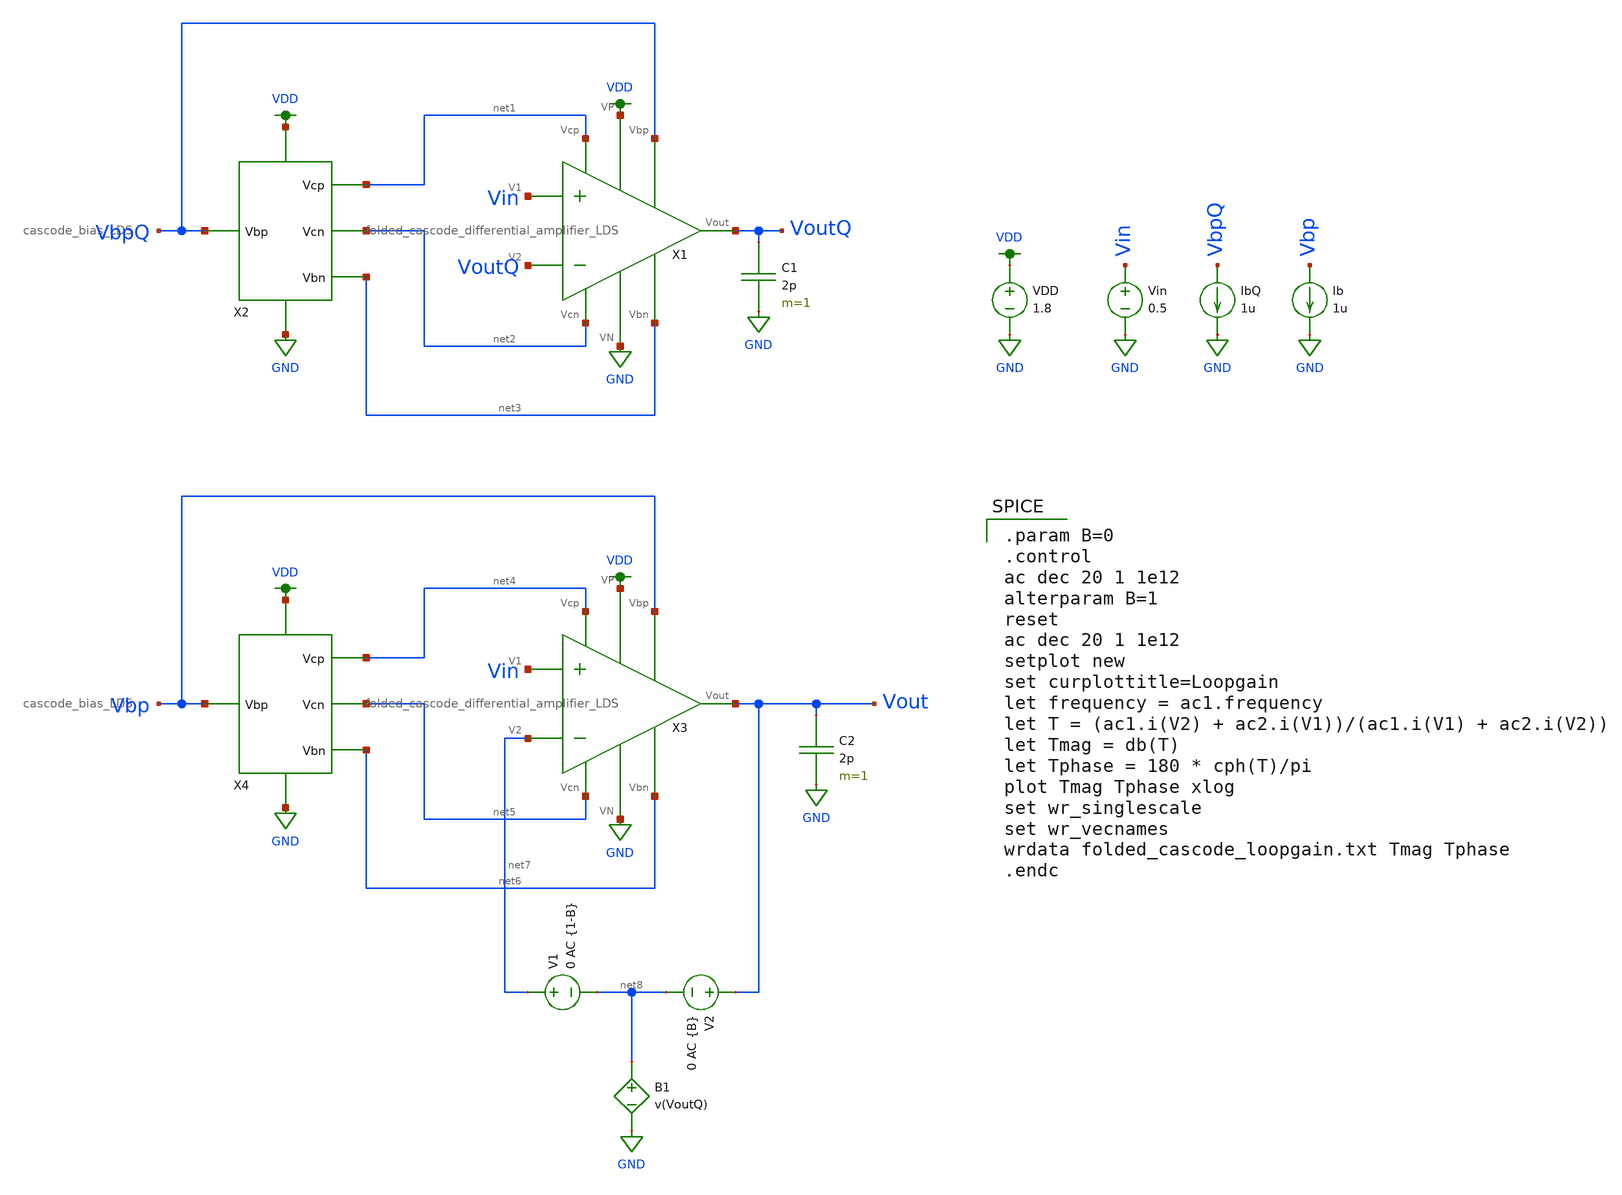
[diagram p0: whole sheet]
** sch_path: schematic/folded_cascode_loopgain_simulation.sch
**.subckt folded_cascode_loopgain_simulation
X1 VDD VbpQ net1 VoutQ net3 net2 Vin VoutQ GND folded_cascode_differential_amplifier_LDS
X2 VDD net1 VbpQ net2 net3 GND cascode_bias_LDS
VDD VDD GND 1.8
Vin Vin GND 0.5
IbQ VbpQ GND 1u
C1 VoutQ GND 2p m=1
Ib Vbp GND 1u
X3 VDD Vbp net4 Vout net6 net5 Vin net7 GND folded_cascode_differential_amplifier_LDS
X4 VDD net4 Vbp net5 net6 GND cascode_bias_LDS
C2 Vout GND 2p m=1
V1 net7 net8 0 AC {1-B}
V2 Vout net8 0 AC {B}
B1 net8 GND V=v(VoutQ)
**** begin user architecture code

.option wnflag=1
.lib ~/skywater/skywater-pdk/libraries/sky130_fd_pr_ngspice/latest/models/sky130.lib.spice tt


.param B=0
.control
ac dec 20 1 1e12
alterparam B=1
reset
ac dec 20 1 1e12
setplot new
set curplottitle=Loopgain
let frequency = ac1.frequency
let T = (ac1.i(V2) + ac2.i(V1))/(ac1.i(V1) + ac2.i(V2))
let Tmag = db(T)
let Tphase = 180 * cph(T)/pi
plot Tmag Tphase xlog
set wr_singlescale
set wr_vecnames
wrdata folded_cascode_loopgain.txt Tmag Tphase
.endc

**** end user architecture code
**.ends

* expanding   symbol:
*+  /home/madvlsi/Documents/MADVLSI-MP3/schematic/folded_cascode_differential_amplifier_LDS.sym # of pins=9
** sym_path: schematic/folded_cascode_differential_amplifier_LDS.sym
** sch_path: schematic/folded_cascode_differential_amplifier_LDS.sch
.subckt folded_cascode_differential_amplifier_LDS VP Vbp Vcp Vout Vbn Vcn V1 V2 VN
*.ipin Vbn
*.ipin Vcn
*.ipin Vcp
*.ipin V2
*.ipin V1
*.ipin Vbp
*.iopin Vp
*.iopin Vn
*.opin Vout
XM11 net3 Vcn net6 GND sky130_fd_pr__nfet_01v8 L=0.5 W=12 nf=1 ad='int((nf+1)/2) * W/nf * 0.29' as='int((nf+2)/2) * W/nf * 0.29'
+ pd='2*int((nf+1)/2) * (W/nf + 0.29)' ps='2*int((nf+2)/2) * (W/nf + 0.29)' nrd='0.29 / W' nrs='0.29 / W'
+ sa=0 sb=0 sd=0 mult=1 m=1
XM12 net3 V1 net1 VDD sky130_fd_pr__pfet_01v8 L=0.5 W=12 nf=1 ad='int((nf+1)/2) * W/nf * 0.29' as='int((nf+2)/2) * W/nf * 0.29'
+ pd='2*int((nf+1)/2) * (W/nf + 0.29)' ps='2*int((nf+2)/2) * (W/nf + 0.29)' nrd='0.29 / W' nrs='0.29 / W'
+ sa=0 sb=0 sd=0 mult=1 m=1
XM13 net2 V2 net1 VDD sky130_fd_pr__pfet_01v8 L=0.5 W=12 nf=1 ad='int((nf+1)/2) * W/nf * 0.29' as='int((nf+2)/2) * W/nf * 0.29'
+ pd='2*int((nf+1)/2) * (W/nf + 0.29)' ps='2*int((nf+2)/2) * (W/nf + 0.29)' nrd='0.29 / W' nrs='0.29 / W'
+ sa=0 sb=0 sd=0 mult=1 m=1
XM14 net1 V2 net2 VDD sky130_fd_pr__pfet_01v8 L=0.5 W=12 nf=1 ad='int((nf+1)/2) * W/nf * 0.29' as='int((nf+2)/2) * W/nf * 0.29'
+ pd='2*int((nf+1)/2) * (W/nf + 0.29)' ps='2*int((nf+2)/2) * (W/nf + 0.29)' nrd='0.29 / W' nrs='0.29 / W'
+ sa=0 sb=0 sd=0 mult=1 m=1
XM15 net1 V1 net3 VDD sky130_fd_pr__pfet_01v8 L=0.5 W=12 nf=1 ad='int((nf+1)/2) * W/nf * 0.29' as='int((nf+2)/2) * W/nf * 0.29'
+ pd='2*int((nf+1)/2) * (W/nf + 0.29)' ps='2*int((nf+2)/2) * (W/nf + 0.29)' nrd='0.29 / W' nrs='0.29 / W'
+ sa=0 sb=0 sd=0 mult=1 m=1
XM16 net3 V1 net1 VDD sky130_fd_pr__pfet_01v8 L=0.5 W=12 nf=1 ad='int((nf+1)/2) * W/nf * 0.29' as='int((nf+2)/2) * W/nf * 0.29'
+ pd='2*int((nf+1)/2) * (W/nf + 0.29)' ps='2*int((nf+2)/2) * (W/nf + 0.29)' nrd='0.29 / W' nrs='0.29 / W'
+ sa=0 sb=0 sd=0 mult=1 m=1
XM17 net2 V2 net1 VDD sky130_fd_pr__pfet_01v8 L=0.5 W=12 nf=1 ad='int((nf+1)/2) * W/nf * 0.29' as='int((nf+2)/2) * W/nf * 0.29'
+ pd='2*int((nf+1)/2) * (W/nf + 0.29)' ps='2*int((nf+2)/2) * (W/nf + 0.29)' nrd='0.29 / W' nrs='0.29 / W'
+ sa=0 sb=0 sd=0 mult=1 m=1
XM18 net1 V2 net2 VDD sky130_fd_pr__pfet_01v8 L=0.5 W=12 nf=1 ad='int((nf+1)/2) * W/nf * 0.29' as='int((nf+2)/2) * W/nf * 0.29'
+ pd='2*int((nf+1)/2) * (W/nf + 0.29)' ps='2*int((nf+2)/2) * (W/nf + 0.29)' nrd='0.29 / W' nrs='0.29 / W'
+ sa=0 sb=0 sd=0 mult=1 m=1
XM19 net1 V1 net3 VDD sky130_fd_pr__pfet_01v8 L=0.5 W=12 nf=1 ad='int((nf+1)/2) * W/nf * 0.29' as='int((nf+2)/2) * W/nf * 0.29'
+ pd='2*int((nf+1)/2) * (W/nf + 0.29)' ps='2*int((nf+2)/2) * (W/nf + 0.29)' nrd='0.29 / W' nrs='0.29 / W'
+ sa=0 sb=0 sd=0 mult=1 m=1
XM20 Vp Vbp net1 VDD sky130_fd_pr__pfet_01v8 L=0.5 W=12 nf=1 ad='int((nf+1)/2) * W/nf * 0.29' as='int((nf+2)/2) * W/nf * 0.29'
+ pd='2*int((nf+1)/2) * (W/nf + 0.29)' ps='2*int((nf+2)/2) * (W/nf + 0.29)' nrd='0.29 / W' nrs='0.29 / W'
+ sa=0 sb=0 sd=0 mult=1 m=1
XM21 net1 Vbp Vp VDD sky130_fd_pr__pfet_01v8 L=0.5 W=12 nf=1 ad='int((nf+1)/2) * W/nf * 0.29' as='int((nf+2)/2) * W/nf * 0.29'
+ pd='2*int((nf+1)/2) * (W/nf + 0.29)' ps='2*int((nf+2)/2) * (W/nf + 0.29)' nrd='0.29 / W' nrs='0.29 / W'
+ sa=0 sb=0 sd=0 mult=1 m=1
XM22 Vp Vbp net1 VDD sky130_fd_pr__pfet_01v8 L=0.5 W=12 nf=1 ad='int((nf+1)/2) * W/nf * 0.29' as='int((nf+2)/2) * W/nf * 0.29'
+ pd='2*int((nf+1)/2) * (W/nf + 0.29)' ps='2*int((nf+2)/2) * (W/nf + 0.29)' nrd='0.29 / W' nrs='0.29 / W'
+ sa=0 sb=0 sd=0 mult=1 m=1
XM23 net1 Vbp Vp VDD sky130_fd_pr__pfet_01v8 L=0.5 W=12 nf=1 ad='int((nf+1)/2) * W/nf * 0.29' as='int((nf+2)/2) * W/nf * 0.29'
+ pd='2*int((nf+1)/2) * (W/nf + 0.29)' ps='2*int((nf+2)/2) * (W/nf + 0.29)' nrd='0.29 / W' nrs='0.29 / W'
+ sa=0 sb=0 sd=0 mult=1 m=1
XM24 Vp Vbp net1 VDD sky130_fd_pr__pfet_01v8 L=0.5 W=12 nf=1 ad='int((nf+1)/2) * W/nf * 0.29' as='int((nf+2)/2) * W/nf * 0.29'
+ pd='2*int((nf+1)/2) * (W/nf + 0.29)' ps='2*int((nf+2)/2) * (W/nf + 0.29)' nrd='0.29 / W' nrs='0.29 / W'
+ sa=0 sb=0 sd=0 mult=1 m=1
XM25 net1 Vbp Vp VDD sky130_fd_pr__pfet_01v8 L=0.5 W=12 nf=1 ad='int((nf+1)/2) * W/nf * 0.29' as='int((nf+2)/2) * W/nf * 0.29'
+ pd='2*int((nf+1)/2) * (W/nf + 0.29)' ps='2*int((nf+2)/2) * (W/nf + 0.29)' nrd='0.29 / W' nrs='0.29 / W'
+ sa=0 sb=0 sd=0 mult=1 m=1
XM26 Vp Vbp net1 VDD sky130_fd_pr__pfet_01v8 L=0.5 W=12 nf=1 ad='int((nf+1)/2) * W/nf * 0.29' as='int((nf+2)/2) * W/nf * 0.29'
+ pd='2*int((nf+1)/2) * (W/nf + 0.29)' ps='2*int((nf+2)/2) * (W/nf + 0.29)' nrd='0.29 / W' nrs='0.29 / W'
+ sa=0 sb=0 sd=0 mult=1 m=1
XM27 net1 Vbp Vp VDD sky130_fd_pr__pfet_01v8 L=0.5 W=12 nf=1 ad='int((nf+1)/2) * W/nf * 0.29' as='int((nf+2)/2) * W/nf * 0.29'
+ pd='2*int((nf+1)/2) * (W/nf + 0.29)' ps='2*int((nf+2)/2) * (W/nf + 0.29)' nrd='0.29 / W' nrs='0.29 / W'
+ sa=0 sb=0 sd=0 mult=1 m=1
XM36 Vn Vbn net3 GND sky130_fd_pr__nfet_01v8 L=0.5 W=12 nf=1 ad='int((nf+1)/2) * W/nf * 0.29' as='int((nf+2)/2) * W/nf * 0.29'
+ pd='2*int((nf+1)/2) * (W/nf + 0.29)' ps='2*int((nf+2)/2) * (W/nf + 0.29)' nrd='0.29 / W' nrs='0.29 / W'
+ sa=0 sb=0 sd=0 mult=1 m=1
XM37 net2 Vbn Vn GND sky130_fd_pr__nfet_01v8 L=0.5 W=12 nf=1 ad='int((nf+1)/2) * W/nf * 0.29' as='int((nf+2)/2) * W/nf * 0.29'
+ pd='2*int((nf+1)/2) * (W/nf + 0.29)' ps='2*int((nf+2)/2) * (W/nf + 0.29)' nrd='0.29 / W' nrs='0.29 / W'
+ sa=0 sb=0 sd=0 mult=1 m=1
XM38 Vout Vcn net2 GND sky130_fd_pr__nfet_01v8 L=0.5 W=12 nf=1 ad='int((nf+1)/2) * W/nf * 0.29' as='int((nf+2)/2) * W/nf * 0.29'
+ pd='2*int((nf+1)/2) * (W/nf + 0.29)' ps='2*int((nf+2)/2) * (W/nf + 0.29)' nrd='0.29 / W' nrs='0.29 / W'
+ sa=0 sb=0 sd=0 mult=1 m=1
XM39 net2 Vcn Vout GND sky130_fd_pr__nfet_01v8 L=0.5 W=12 nf=1 ad='int((nf+1)/2) * W/nf * 0.29' as='int((nf+2)/2) * W/nf * 0.29'
+ pd='2*int((nf+1)/2) * (W/nf + 0.29)' ps='2*int((nf+2)/2) * (W/nf + 0.29)' nrd='0.29 / W' nrs='0.29 / W'
+ sa=0 sb=0 sd=0 mult=1 m=1
XM40 Vn Vbn net2 GND sky130_fd_pr__nfet_01v8 L=0.5 W=12 nf=1 ad='int((nf+1)/2) * W/nf * 0.29' as='int((nf+2)/2) * W/nf * 0.29'
+ pd='2*int((nf+1)/2) * (W/nf + 0.29)' ps='2*int((nf+2)/2) * (W/nf + 0.29)' nrd='0.29 / W' nrs='0.29 / W'
+ sa=0 sb=0 sd=0 mult=1 m=1
XM41 net3 Vbn Vn GND sky130_fd_pr__nfet_01v8 L=0.5 W=12 nf=1 ad='int((nf+1)/2) * W/nf * 0.29' as='int((nf+2)/2) * W/nf * 0.29'
+ pd='2*int((nf+1)/2) * (W/nf + 0.29)' ps='2*int((nf+2)/2) * (W/nf + 0.29)' nrd='0.29 / W' nrs='0.29 / W'
+ sa=0 sb=0 sd=0 mult=1 m=1
XM42 net6 Vcn net3 GND sky130_fd_pr__nfet_01v8 L=0.5 W=12 nf=1 ad='int((nf+1)/2) * W/nf * 0.29' as='int((nf+2)/2) * W/nf * 0.29'
+ pd='2*int((nf+1)/2) * (W/nf + 0.29)' ps='2*int((nf+2)/2) * (W/nf + 0.29)' nrd='0.29 / W' nrs='0.29 / W'
+ sa=0 sb=0 sd=0 mult=1 m=1
XM44 Vout Vcp net4 VDD sky130_fd_pr__pfet_01v8 L=0.5 W=12 nf=1 ad='int((nf+1)/2) * W/nf * 0.29' as='int((nf+2)/2) * W/nf * 0.29'
+ pd='2*int((nf+1)/2) * (W/nf + 0.29)' ps='2*int((nf+2)/2) * (W/nf + 0.29)' nrd='0.29 / W' nrs='0.29 / W'
+ sa=0 sb=0 sd=0 mult=1 m=1
XM45 net4 net6 Vp VDD sky130_fd_pr__pfet_01v8 L=0.5 W=12 nf=1 ad='int((nf+1)/2) * W/nf * 0.29' as='int((nf+2)/2) * W/nf * 0.29'
+ pd='2*int((nf+1)/2) * (W/nf + 0.29)' ps='2*int((nf+2)/2) * (W/nf + 0.29)' nrd='0.29 / W' nrs='0.29 / W'
+ sa=0 sb=0 sd=0 mult=1 m=1
XM46 Vp net6 net5 VDD sky130_fd_pr__pfet_01v8 L=0.5 W=12 nf=1 ad='int((nf+1)/2) * W/nf * 0.29' as='int((nf+2)/2) * W/nf * 0.29'
+ pd='2*int((nf+1)/2) * (W/nf + 0.29)' ps='2*int((nf+2)/2) * (W/nf + 0.29)' nrd='0.29 / W' nrs='0.29 / W'
+ sa=0 sb=0 sd=0 mult=1 m=1
XM47 net5 Vcp net6 VDD sky130_fd_pr__pfet_01v8 L=0.5 W=12 nf=1 ad='int((nf+1)/2) * W/nf * 0.29' as='int((nf+2)/2) * W/nf * 0.29'
+ pd='2*int((nf+1)/2) * (W/nf + 0.29)' ps='2*int((nf+2)/2) * (W/nf + 0.29)' nrd='0.29 / W' nrs='0.29 / W'
+ sa=0 sb=0 sd=0 mult=1 m=1
XM48 net6 Vcp net5 VDD sky130_fd_pr__pfet_01v8 L=0.5 W=12 nf=1 ad='int((nf+1)/2) * W/nf * 0.29' as='int((nf+2)/2) * W/nf * 0.29'
+ pd='2*int((nf+1)/2) * (W/nf + 0.29)' ps='2*int((nf+2)/2) * (W/nf + 0.29)' nrd='0.29 / W' nrs='0.29 / W'
+ sa=0 sb=0 sd=0 mult=1 m=1
XM49 net5 net6 Vp VDD sky130_fd_pr__pfet_01v8 L=0.5 W=12 nf=1 ad='int((nf+1)/2) * W/nf * 0.29' as='int((nf+2)/2) * W/nf * 0.29'
+ pd='2*int((nf+1)/2) * (W/nf + 0.29)' ps='2*int((nf+2)/2) * (W/nf + 0.29)' nrd='0.29 / W' nrs='0.29 / W'
+ sa=0 sb=0 sd=0 mult=1 m=1
XM50 Vp net6 net4 VDD sky130_fd_pr__pfet_01v8 L=0.5 W=12 nf=1 ad='int((nf+1)/2) * W/nf * 0.29' as='int((nf+2)/2) * W/nf * 0.29'
+ pd='2*int((nf+1)/2) * (W/nf + 0.29)' ps='2*int((nf+2)/2) * (W/nf + 0.29)' nrd='0.29 / W' nrs='0.29 / W'
+ sa=0 sb=0 sd=0 mult=1 m=1
XM51 net4 Vcp Vout VDD sky130_fd_pr__pfet_01v8 L=0.5 W=12 nf=1 ad='int((nf+1)/2) * W/nf * 0.29' as='int((nf+2)/2) * W/nf * 0.29'
+ pd='2*int((nf+1)/2) * (W/nf + 0.29)' ps='2*int((nf+2)/2) * (W/nf + 0.29)' nrd='0.29 / W' nrs='0.29 / W'
+ sa=0 sb=0 sd=0 mult=1 m=1
.ends


* expanding   symbol:  /home/madvlsi/Documents/MADVLSI-MP3/schematic/cascode_bias_LDS.sym # of
*+ pins=6
** sym_path: schematic/cascode_bias_LDS.sym
** sch_path: schematic/cascode_bias_LDS.sch
.subckt cascode_bias_LDS VP Vcp Vbp Vcn Vbn VN
*.iopin VP
*.iopin VN
*.opin Vcp
*.opin Vbn
*.opin Vcn
*.iopin Vbp
XM1a VP Vbp Vbp VDD sky130_fd_pr__pfet_01v8 L=0.5 W=6 nf=1 ad='int((nf+1)/2) * W/nf * 0.29' as='int((nf+2)/2) * W/nf * 0.29'
+ pd='2*int((nf+1)/2) * (W/nf + 0.29)' ps='2*int((nf+2)/2) * (W/nf + 0.29)' nrd='0.29 / W' nrs='0.29 / W'
+ sa=0 sb=0 sd=0 mult=1 m=1
XM2a Vbn Vbp VP VDD sky130_fd_pr__pfet_01v8 L=0.5 W=6 nf=1 ad='int((nf+1)/2) * W/nf * 0.29' as='int((nf+2)/2) * W/nf * 0.29'
+ pd='2*int((nf+1)/2) * (W/nf + 0.29)' ps='2*int((nf+2)/2) * (W/nf + 0.29)' nrd='0.29 / W' nrs='0.29 / W'
+ sa=0 sb=0 sd=0 mult=1 m=1
XM3a VP Vbp Vcn VDD sky130_fd_pr__pfet_01v8 L=0.5 W=6 nf=1 ad='int((nf+1)/2) * W/nf * 0.29' as='int((nf+2)/2) * W/nf * 0.29'
+ pd='2*int((nf+1)/2) * (W/nf + 0.29)' ps='2*int((nf+2)/2) * (W/nf + 0.29)' nrd='0.29 / W' nrs='0.29 / W'
+ sa=0 sb=0 sd=0 mult=1 m=1
XM4a net1 Vbp VP VDD sky130_fd_pr__pfet_01v8 L=0.5 W=6 nf=1 ad='int((nf+1)/2) * W/nf * 0.29' as='int((nf+2)/2) * W/nf * 0.29'
+ pd='2*int((nf+1)/2) * (W/nf + 0.29)' ps='2*int((nf+2)/2) * (W/nf + 0.29)' nrd='0.29 / W' nrs='0.29 / W'
+ sa=0 sb=0 sd=0 mult=1 m=1
XM4c net2 Vbp net3 VDD sky130_fd_pr__pfet_01v8 L=0.5 W=6 nf=1 ad='int((nf+1)/2) * W/nf * 0.29' as='int((nf+2)/2) * W/nf * 0.29'
+ pd='2*int((nf+1)/2) * (W/nf + 0.29)' ps='2*int((nf+2)/2) * (W/nf + 0.29)' nrd='0.29 / W' nrs='0.29 / W'
+ sa=0 sb=0 sd=0 mult=1 m=1
XM3b Vcn Vbp VP VDD sky130_fd_pr__pfet_01v8 L=0.5 W=6 nf=1 ad='int((nf+1)/2) * W/nf * 0.29' as='int((nf+2)/2) * W/nf * 0.29'
+ pd='2*int((nf+1)/2) * (W/nf + 0.29)' ps='2*int((nf+2)/2) * (W/nf + 0.29)' nrd='0.29 / W' nrs='0.29 / W'
+ sa=0 sb=0 sd=0 mult=1 m=1
XM2b VP Vbp Vbn VDD sky130_fd_pr__pfet_01v8 L=0.5 W=6 nf=1 ad='int((nf+1)/2) * W/nf * 0.29' as='int((nf+2)/2) * W/nf * 0.29'
+ pd='2*int((nf+1)/2) * (W/nf + 0.29)' ps='2*int((nf+2)/2) * (W/nf + 0.29)' nrd='0.29 / W' nrs='0.29 / W'
+ sa=0 sb=0 sd=0 mult=1 m=1
XM1b Vbp Vbp VP VDD sky130_fd_pr__pfet_01v8 L=0.5 W=6 nf=1 ad='int((nf+1)/2) * W/nf * 0.29' as='int((nf+2)/2) * W/nf * 0.29'
+ pd='2*int((nf+1)/2) * (W/nf + 0.29)' ps='2*int((nf+2)/2) * (W/nf + 0.29)' nrd='0.29 / W' nrs='0.29 / W'
+ sa=0 sb=0 sd=0 mult=1 m=1
XM6a net5 net5 net4 VDD sky130_fd_pr__pfet_01v8 L=0.5 W=6 nf=1 ad='int((nf+1)/2) * W/nf * 0.29' as='int((nf+2)/2) * W/nf * 0.29'
+ pd='2*int((nf+1)/2) * (W/nf + 0.29)' ps='2*int((nf+2)/2) * (W/nf + 0.29)' nrd='0.29 / W' nrs='0.29 / W'
+ sa=0 sb=0 sd=0 mult=1 m=1
XM6b net5 net5 net5 VDD sky130_fd_pr__pfet_01v8 L=0.5 W=6 nf=1 ad='int((nf+1)/2) * W/nf * 0.29' as='int((nf+2)/2) * W/nf * 0.29'
+ pd='2*int((nf+1)/2) * (W/nf + 0.29)' ps='2*int((nf+2)/2) * (W/nf + 0.29)' nrd='0.29 / W' nrs='0.29 / W'
+ sa=0 sb=0 sd=0 mult=1 m=1
XM5a Vcp Vcp net4 VDD sky130_fd_pr__pfet_01v8 L=0.5 W=6 nf=1 ad='int((nf+1)/2) * W/nf * 0.29' as='int((nf+2)/2) * W/nf * 0.29'
+ pd='2*int((nf+1)/2) * (W/nf + 0.29)' ps='2*int((nf+2)/2) * (W/nf + 0.29)' nrd='0.29 / W' nrs='0.29 / W'
+ sa=0 sb=0 sd=0 mult=1 m=1
XM5b net4 Vcp Vcp VDD sky130_fd_pr__pfet_01v8 L=0.5 W=6 nf=1 ad='int((nf+1)/2) * W/nf * 0.29' as='int((nf+2)/2) * W/nf * 0.29'
+ pd='2*int((nf+1)/2) * (W/nf + 0.29)' ps='2*int((nf+2)/2) * (W/nf + 0.29)' nrd='0.29 / W' nrs='0.29 / W'
+ sa=0 sb=0 sd=0 mult=1 m=1
XM6c net5 net5 net5 VDD sky130_fd_pr__pfet_01v8 L=0.5 W=6 nf=1 ad='int((nf+1)/2) * W/nf * 0.29' as='int((nf+2)/2) * W/nf * 0.29'
+ pd='2*int((nf+1)/2) * (W/nf + 0.29)' ps='2*int((nf+2)/2) * (W/nf + 0.29)' nrd='0.29 / W' nrs='0.29 / W'
+ sa=0 sb=0 sd=0 mult=1 m=1
XM6d net4 net5 net5 VDD sky130_fd_pr__pfet_01v8 L=0.5 W=6 nf=1 ad='int((nf+1)/2) * W/nf * 0.29' as='int((nf+2)/2) * W/nf * 0.29'
+ pd='2*int((nf+1)/2) * (W/nf + 0.29)' ps='2*int((nf+2)/2) * (W/nf + 0.29)' nrd='0.29 / W' nrs='0.29 / W'
+ sa=0 sb=0 sd=0 mult=1 m=1
XM8a Vcp Vbn VN GND sky130_fd_pr__nfet_01v8 L=0.5 W=6 nf=1 ad='int((nf+1)/2) * W/nf * 0.29' as='int((nf+2)/2) * W/nf * 0.29'
+ pd='2*int((nf+1)/2) * (W/nf + 0.29)' ps='2*int((nf+2)/2) * (W/nf + 0.29)' nrd='0.29 / W' nrs='0.29 / W'
+ sa=0 sb=0 sd=0 mult=1 m=1
XM8b VN Vbn Vcp GND sky130_fd_pr__nfet_01v8 L=0.5 W=6 nf=1 ad='int((nf+1)/2) * W/nf * 0.29' as='int((nf+2)/2) * W/nf * 0.29'
+ pd='2*int((nf+1)/2) * (W/nf + 0.29)' ps='2*int((nf+2)/2) * (W/nf + 0.29)' nrd='0.29 / W' nrs='0.29 / W'
+ sa=0 sb=0 sd=0 mult=1 m=1
XM10b VN Vbn net6 GND sky130_fd_pr__nfet_01v8 L=0.5 W=6 nf=1 ad='int((nf+1)/2) * W/nf * 0.29' as='int((nf+2)/2) * W/nf * 0.29'
+ pd='2*int((nf+1)/2) * (W/nf + 0.29)' ps='2*int((nf+2)/2) * (W/nf + 0.29)' nrd='0.29 / W' nrs='0.29 / W'
+ sa=0 sb=0 sd=0 mult=1 m=1
XM9a Vbn Vbn VN GND sky130_fd_pr__nfet_01v8 L=0.5 W=6 nf=1 ad='int((nf+1)/2) * W/nf * 0.29' as='int((nf+2)/2) * W/nf * 0.29'
+ pd='2*int((nf+1)/2) * (W/nf + 0.29)' ps='2*int((nf+2)/2) * (W/nf + 0.29)' nrd='0.29 / W' nrs='0.29 / W'
+ sa=0 sb=0 sd=0 mult=1 m=1
XM9b VN Vbn Vbn GND sky130_fd_pr__nfet_01v8 L=0.5 W=6 nf=1 ad='int((nf+1)/2) * W/nf * 0.29' as='int((nf+2)/2) * W/nf * 0.29'
+ pd='2*int((nf+1)/2) * (W/nf + 0.29)' ps='2*int((nf+2)/2) * (W/nf + 0.29)' nrd='0.29 / W' nrs='0.29 / W'
+ sa=0 sb=0 sd=0 mult=1 m=1
XM10c net6 Vbn VN GND sky130_fd_pr__nfet_01v8 L=0.5 W=6 nf=1 ad='int((nf+1)/2) * W/nf * 0.29' as='int((nf+2)/2) * W/nf * 0.29'
+ pd='2*int((nf+1)/2) * (W/nf + 0.29)' ps='2*int((nf+2)/2) * (W/nf + 0.29)' nrd='0.29 / W' nrs='0.29 / W'
+ sa=0 sb=0 sd=0 mult=1 m=1
XM11a Vcn Vcn net7 GND sky130_fd_pr__nfet_01v8 L=0.5 W=6 nf=1 ad='int((nf+1)/2) * W/nf * 0.29' as='int((nf+2)/2) * W/nf * 0.29'
+ pd='2*int((nf+1)/2) * (W/nf + 0.29)' ps='2*int((nf+2)/2) * (W/nf + 0.29)' nrd='0.29 / W' nrs='0.29 / W'
+ sa=0 sb=0 sd=0 mult=1 m=1
XM11b net7 Vcn Vcn GND sky130_fd_pr__nfet_01v8 L=0.5 W=6 nf=1 ad='int((nf+1)/2) * W/nf * 0.29' as='int((nf+2)/2) * W/nf * 0.29'
+ pd='2*int((nf+1)/2) * (W/nf + 0.29)' ps='2*int((nf+2)/2) * (W/nf + 0.29)' nrd='0.29 / W' nrs='0.29 / W'
+ sa=0 sb=0 sd=0 mult=1 m=1
XM13a net7 net3 VN GND sky130_fd_pr__nfet_01v8 L=0.5 W=6 nf=1 ad='int((nf+1)/2) * W/nf * 0.29' as='int((nf+2)/2) * W/nf * 0.29'
+ pd='2*int((nf+1)/2) * (W/nf + 0.29)' ps='2*int((nf+2)/2) * (W/nf + 0.29)' nrd='0.29 / W' nrs='0.29 / W'
+ sa=0 sb=0 sd=0 mult=1 m=1
XM12a net3 net3 net7 GND sky130_fd_pr__nfet_01v8 L=0.5 W=6 nf=1 ad='int((nf+1)/2) * W/nf * 0.29' as='int((nf+2)/2) * W/nf * 0.29'
+ pd='2*int((nf+1)/2) * (W/nf + 0.29)' ps='2*int((nf+2)/2) * (W/nf + 0.29)' nrd='0.29 / W' nrs='0.29 / W'
+ sa=0 sb=0 sd=0 mult=1 m=1
XM12d net7 net3 net3 GND sky130_fd_pr__nfet_01v8 L=0.5 W=6 nf=1 ad='int((nf+1)/2) * W/nf * 0.29' as='int((nf+2)/2) * W/nf * 0.29'
+ pd='2*int((nf+1)/2) * (W/nf + 0.29)' ps='2*int((nf+2)/2) * (W/nf + 0.29)' nrd='0.29 / W' nrs='0.29 / W'
+ sa=0 sb=0 sd=0 mult=1 m=1
XM13b VN net3 net7 GND sky130_fd_pr__nfet_01v8 L=0.5 W=6 nf=1 ad='int((nf+1)/2) * W/nf * 0.29' as='int((nf+2)/2) * W/nf * 0.29'
+ pd='2*int((nf+1)/2) * (W/nf + 0.29)' ps='2*int((nf+2)/2) * (W/nf + 0.29)' nrd='0.29 / W' nrs='0.29 / W'
+ sa=0 sb=0 sd=0 mult=1 m=1
XM15 Vbp VP VP VDD sky130_fd_pr__pfet_01v8 L=0.5 W=6 nf=1 ad='int((nf+1)/2) * W/nf * 0.29' as='int((nf+2)/2) * W/nf * 0.29'
+ pd='2*int((nf+1)/2) * (W/nf + 0.29)' ps='2*int((nf+2)/2) * (W/nf + 0.29)' nrd='0.29 / W' nrs='0.29 / W'
+ sa=0 sb=0 sd=0 mult=1 m=1
XM25 VN VN VN GND sky130_fd_pr__nfet_01v8 L=0.5 W=6 nf=1 ad='int((nf+1)/2) * W/nf * 0.29' as='int((nf+2)/2) * W/nf * 0.29'
+ pd='2*int((nf+1)/2) * (W/nf + 0.29)' ps='2*int((nf+2)/2) * (W/nf + 0.29)' nrd='0.29 / W' nrs='0.29 / W'
+ sa=0 sb=0 sd=0 mult=1 m=1
XM24 VN VN VN GND sky130_fd_pr__nfet_01v8 L=0.5 W=6 nf=1 ad='int((nf+1)/2) * W/nf * 0.29' as='int((nf+2)/2) * W/nf * 0.29'
+ pd='2*int((nf+1)/2) * (W/nf + 0.29)' ps='2*int((nf+2)/2) * (W/nf + 0.29)' nrd='0.29 / W' nrs='0.29 / W'
+ sa=0 sb=0 sd=0 mult=1 m=1
XM26 VN VN VN GND sky130_fd_pr__nfet_01v8 L=0.5 W=6 nf=1 ad='int((nf+1)/2) * W/nf * 0.29' as='int((nf+2)/2) * W/nf * 0.29'
+ pd='2*int((nf+1)/2) * (W/nf + 0.29)' ps='2*int((nf+2)/2) * (W/nf + 0.29)' nrd='0.29 / W' nrs='0.29 / W'
+ sa=0 sb=0 sd=0 mult=1 m=1
XM27 VN VN VN GND sky130_fd_pr__nfet_01v8 L=0.5 W=6 nf=1 ad='int((nf+1)/2) * W/nf * 0.29' as='int((nf+2)/2) * W/nf * 0.29'
+ pd='2*int((nf+1)/2) * (W/nf + 0.29)' ps='2*int((nf+2)/2) * (W/nf + 0.29)' nrd='0.29 / W' nrs='0.29 / W'
+ sa=0 sb=0 sd=0 mult=1 m=1
XM10a net6 Vbn net5 GND sky130_fd_pr__nfet_01v8 L=0.5 W=6 nf=1 ad='int((nf+1)/2) * W/nf * 0.29' as='int((nf+2)/2) * W/nf * 0.29'
+ pd='2*int((nf+1)/2) * (W/nf + 0.29)' ps='2*int((nf+2)/2) * (W/nf + 0.29)' nrd='0.29 / W' nrs='0.29 / W'
+ sa=0 sb=0 sd=0 mult=1 m=1
XM20 net5 VN VN GND sky130_fd_pr__nfet_01v8 L=0.5 W=6 nf=1 ad='int((nf+1)/2) * W/nf * 0.29' as='int((nf+2)/2) * W/nf * 0.29'
+ pd='2*int((nf+1)/2) * (W/nf + 0.29)' ps='2*int((nf+2)/2) * (W/nf + 0.29)' nrd='0.29 / W' nrs='0.29 / W'
+ sa=0 sb=0 sd=0 mult=1 m=1
XM23 VN VN net5 GND sky130_fd_pr__nfet_01v8 L=0.5 W=6 nf=1 ad='int((nf+1)/2) * W/nf * 0.29' as='int((nf+2)/2) * W/nf * 0.29'
+ pd='2*int((nf+1)/2) * (W/nf + 0.29)' ps='2*int((nf+2)/2) * (W/nf + 0.29)' nrd='0.29 / W' nrs='0.29 / W'
+ sa=0 sb=0 sd=0 mult=1 m=1
XM10d net5 Vbn net6 GND sky130_fd_pr__nfet_01v8 L=0.5 W=6 nf=1 ad='int((nf+1)/2) * W/nf * 0.29' as='int((nf+2)/2) * W/nf * 0.29'
+ pd='2*int((nf+1)/2) * (W/nf + 0.29)' ps='2*int((nf+2)/2) * (W/nf + 0.29)' nrd='0.29 / W' nrs='0.29 / W'
+ sa=0 sb=0 sd=0 mult=1 m=1
XM14 VP VP Vbp VDD sky130_fd_pr__pfet_01v8 L=0.5 W=6 nf=1 ad='int((nf+1)/2) * W/nf * 0.29' as='int((nf+2)/2) * W/nf * 0.29'
+ pd='2*int((nf+1)/2) * (W/nf + 0.29)' ps='2*int((nf+2)/2) * (W/nf + 0.29)' nrd='0.29 / W' nrs='0.29 / W'
+ sa=0 sb=0 sd=0 mult=1 m=1
XM7a net4 net5 VP VDD sky130_fd_pr__pfet_01v8 L=0.5 W=6 nf=1 ad='int((nf+1)/2) * W/nf * 0.29' as='int((nf+2)/2) * W/nf * 0.29'
+ pd='2*int((nf+1)/2) * (W/nf + 0.29)' ps='2*int((nf+2)/2) * (W/nf + 0.29)' nrd='0.29 / W' nrs='0.29 / W'
+ sa=0 sb=0 sd=0 mult=1 m=1
XM16 VP VP VP VDD sky130_fd_pr__pfet_01v8 L=0.5 W=6 nf=1 ad='int((nf+1)/2) * W/nf * 0.29' as='int((nf+2)/2) * W/nf * 0.29'
+ pd='2*int((nf+1)/2) * (W/nf + 0.29)' ps='2*int((nf+2)/2) * (W/nf + 0.29)' nrd='0.29 / W' nrs='0.29 / W'
+ sa=0 sb=0 sd=0 mult=1 m=1
XM7b VP net5 net4 VDD sky130_fd_pr__pfet_01v8 L=0.5 W=6 nf=1 ad='int((nf+1)/2) * W/nf * 0.29' as='int((nf+2)/2) * W/nf * 0.29'
+ pd='2*int((nf+1)/2) * (W/nf + 0.29)' ps='2*int((nf+2)/2) * (W/nf + 0.29)' nrd='0.29 / W' nrs='0.29 / W'
+ sa=0 sb=0 sd=0 mult=1 m=1
XM19 VP VP VP VDD sky130_fd_pr__pfet_01v8 L=0.5 W=6 nf=1 ad='int((nf+1)/2) * W/nf * 0.29' as='int((nf+2)/2) * W/nf * 0.29'
+ pd='2*int((nf+1)/2) * (W/nf + 0.29)' ps='2*int((nf+2)/2) * (W/nf + 0.29)' nrd='0.29 / W' nrs='0.29 / W'
+ sa=0 sb=0 sd=0 mult=1 m=1
XM4b net3 Vbp net1 VDD sky130_fd_pr__pfet_01v8 L=0.5 W=6 nf=1 ad='int((nf+1)/2) * W/nf * 0.29' as='int((nf+2)/2) * W/nf * 0.29'
+ pd='2*int((nf+1)/2) * (W/nf + 0.29)' ps='2*int((nf+2)/2) * (W/nf + 0.29)' nrd='0.29 / W' nrs='0.29 / W'
+ sa=0 sb=0 sd=0 mult=1 m=1
XM4d VP Vbp net2 VDD sky130_fd_pr__pfet_01v8 L=0.5 W=6 nf=1 ad='int((nf+1)/2) * W/nf * 0.29' as='int((nf+2)/2) * W/nf * 0.29'
+ pd='2*int((nf+1)/2) * (W/nf + 0.29)' ps='2*int((nf+2)/2) * (W/nf + 0.29)' nrd='0.29 / W' nrs='0.29 / W'
+ sa=0 sb=0 sd=0 mult=1 m=1
XM3 VP VP VP VDD sky130_fd_pr__pfet_01v8 L=0.5 W=6 nf=1 ad='int((nf+1)/2) * W/nf * 0.29' as='int((nf+2)/2) * W/nf * 0.29'
+ pd='2*int((nf+1)/2) * (W/nf + 0.29)' ps='2*int((nf+2)/2) * (W/nf + 0.29)' nrd='0.29 / W' nrs='0.29 / W'
+ sa=0 sb=0 sd=0 mult=1 m=1
XM4 VP VP VP VDD sky130_fd_pr__pfet_01v8 L=0.5 W=6 nf=1 ad='int((nf+1)/2) * W/nf * 0.29' as='int((nf+2)/2) * W/nf * 0.29'
+ pd='2*int((nf+1)/2) * (W/nf + 0.29)' ps='2*int((nf+2)/2) * (W/nf + 0.29)' nrd='0.29 / W' nrs='0.29 / W'
+ sa=0 sb=0 sd=0 mult=1 m=1
XM5 VN VN VN GND sky130_fd_pr__nfet_01v8 L=0.5 W=6 nf=1 ad='int((nf+1)/2) * W/nf * 0.29' as='int((nf+2)/2) * W/nf * 0.29'
+ pd='2*int((nf+1)/2) * (W/nf + 0.29)' ps='2*int((nf+2)/2) * (W/nf + 0.29)' nrd='0.29 / W' nrs='0.29 / W'
+ sa=0 sb=0 sd=0 mult=1 m=1
XM6 VN VN VN GND sky130_fd_pr__nfet_01v8 L=0.5 W=6 nf=1 ad='int((nf+1)/2) * W/nf * 0.29' as='int((nf+2)/2) * W/nf * 0.29'
+ pd='2*int((nf+1)/2) * (W/nf + 0.29)' ps='2*int((nf+2)/2) * (W/nf + 0.29)' nrd='0.29 / W' nrs='0.29 / W'
+ sa=0 sb=0 sd=0 mult=1 m=1
XM12c net3 net3 net3 GND sky130_fd_pr__nfet_01v8 L=0.5 W=6 nf=1 ad='int((nf+1)/2) * W/nf * 0.29' as='int((nf+2)/2) * W/nf * 0.29'
+ pd='2*int((nf+1)/2) * (W/nf + 0.29)' ps='2*int((nf+2)/2) * (W/nf + 0.29)' nrd='0.29 / W' nrs='0.29 / W'
+ sa=0 sb=0 sd=0 mult=1 m=1
XM12b net3 net3 net3 GND sky130_fd_pr__nfet_01v8 L=0.5 W=6 nf=1 ad='int((nf+1)/2) * W/nf * 0.29' as='int((nf+2)/2) * W/nf * 0.29'
+ pd='2*int((nf+1)/2) * (W/nf + 0.29)' ps='2*int((nf+2)/2) * (W/nf + 0.29)' nrd='0.29 / W' nrs='0.29 / W'
+ sa=0 sb=0 sd=0 mult=1 m=1
.ends

.GLOBAL GND
.GLOBAL VDD
.end
